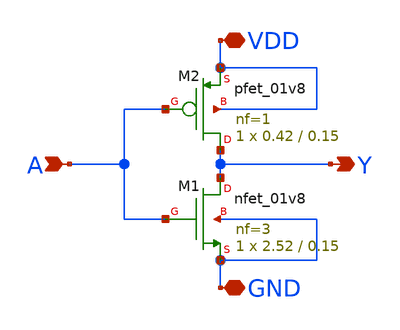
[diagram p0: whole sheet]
** sch_path: cells/INV1X1/schematic/inv1x1.sch
**.subckt inv1x1 A Y VDD GND
*.ipin A
*.opin Y
*.iopin VDD
*.iopin GND
XM1 Y A GND GND sky130_fd_pr__nfet_01v8 L=0.15 W=2.52 nf=3 ad='int((3 + 1)/2) * 2.52 / 3 * 0.29' as='int((3 + 2)/2) * 2.52 / 3 * 0.29'
+ pd='2*int((3 + 1)/2) * (2.52 / 3 + 0.29)' ps='2*int((3 + 2)/2) * (2.52 / 3 + 0.29)' nrd='0.29 / 2.52 '
+ nrs='0.29 / 2.52 ' sa=0 sb=0 sd=0 mult=1 m=1
XM2 Y A VDD VDD sky130_fd_pr__pfet_01v8 L=0.15 W=0.42 nf=1 ad='int((1 + 1)/2) * 0.42 / 1 * 0.29' as='int((1 + 2)/2) * 0.42 / 1 * 0.29'
+ pd='2*int((1 + 1)/2) * (0.42 / 1 + 0.29)' ps='2*int((1 + 2)/2) * (0.42 / 1 + 0.29)' nrd='0.29 / 0.42 '
+ nrs='0.29 / 0.42 ' sa=0 sb=0 sd=0 mult=1 m=1
**.ends
.end
